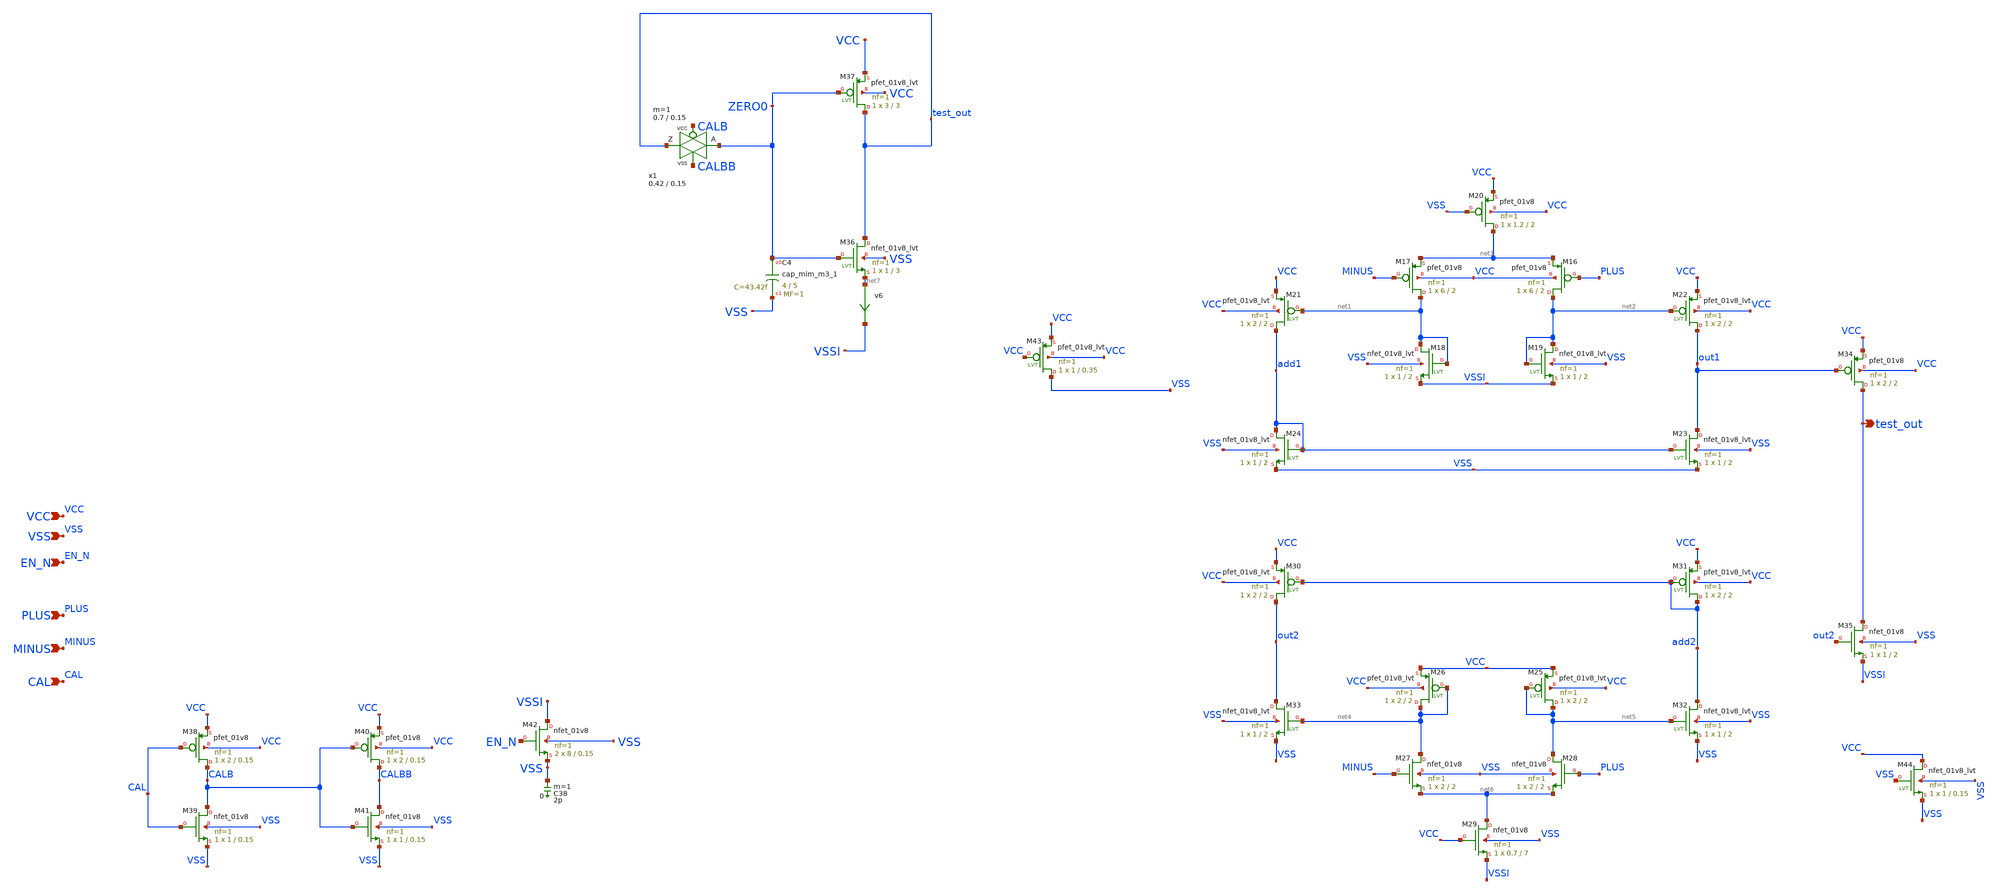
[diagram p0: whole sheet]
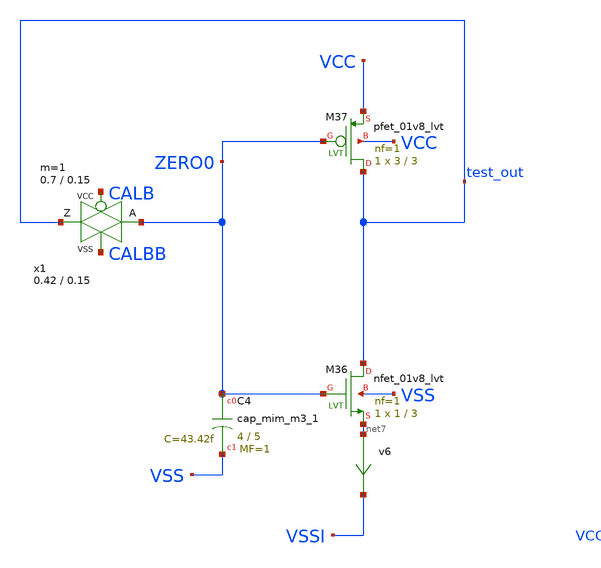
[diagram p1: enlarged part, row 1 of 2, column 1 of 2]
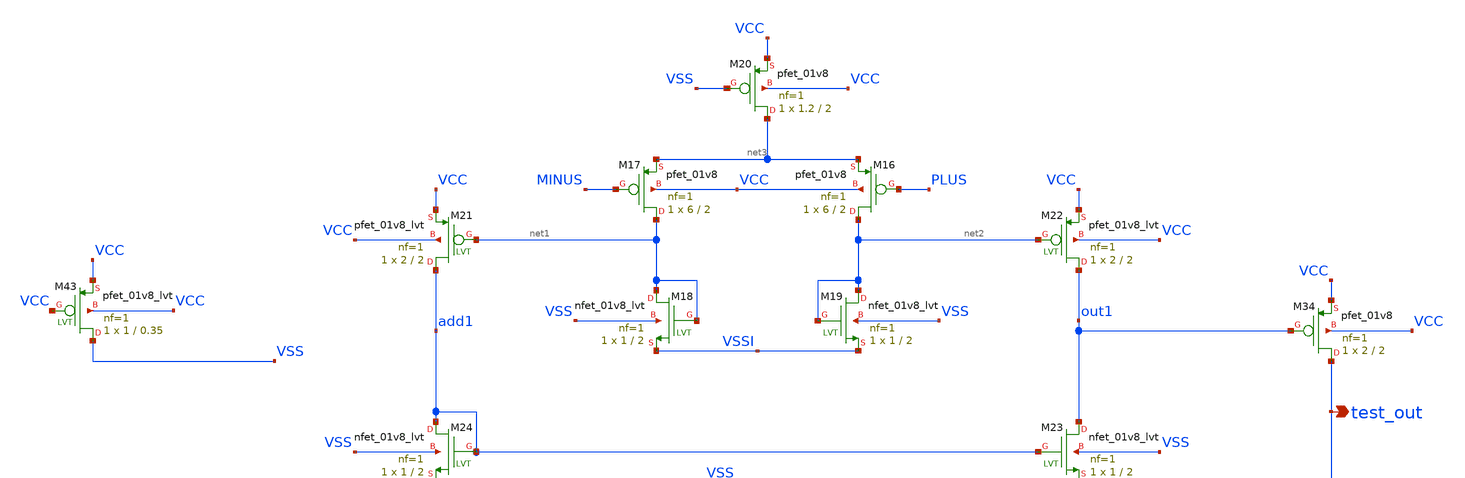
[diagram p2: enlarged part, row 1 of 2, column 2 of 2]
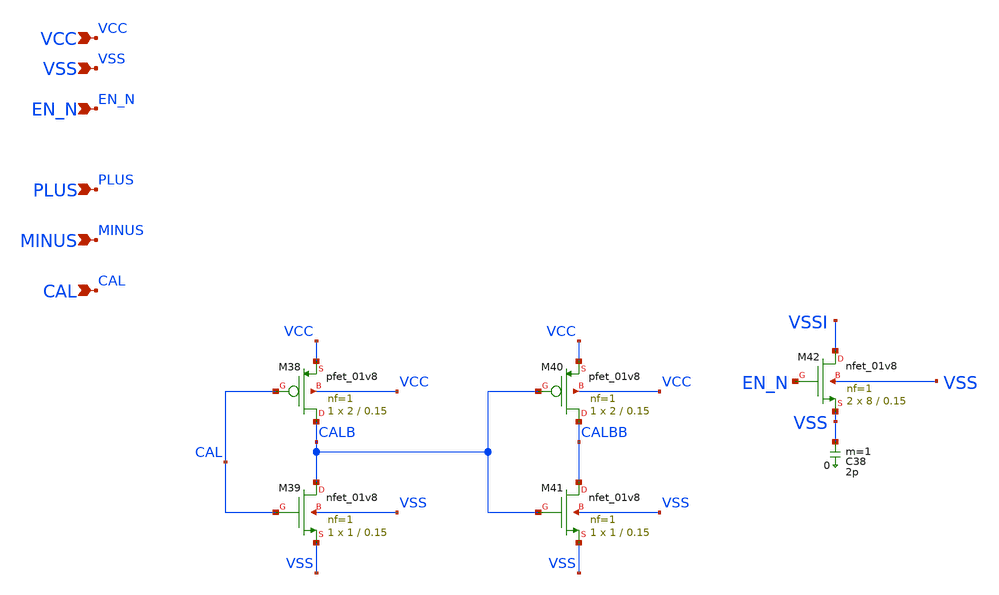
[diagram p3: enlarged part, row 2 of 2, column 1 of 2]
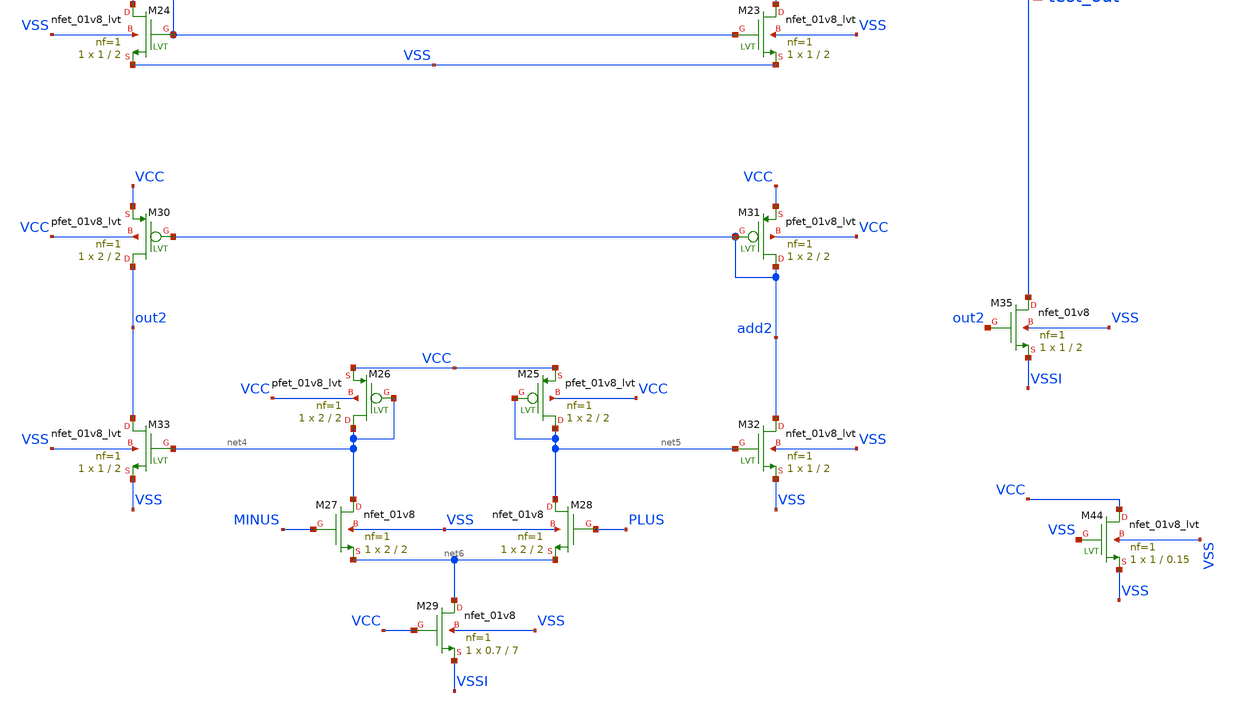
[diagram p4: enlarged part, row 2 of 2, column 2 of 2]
** sch_path: xschem/comparator.sch
**.subckt comparator VCC VSS EN_N PLUS MINUS test_out CAL
*.ipin VCC
*.ipin VSS
*.ipin EN_N
*.ipin PLUS
*.ipin MINUS
*.opin test_out
*.ipin CAL
XM16 net2 PLUS net3 VCC sky130_fd_pr__pfet_01v8 L=2 W=6 nf=1 ad='int((nf+1)/2) * W/nf * 0.29' as='int((nf+2)/2) * W/nf * 0.29'
+ pd='2*int((nf+1)/2) * (W/nf + 0.29)' ps='2*int((nf+2)/2) * (W/nf + 0.29)' nrd='0.29 / W' nrs='0.29 / W'
+ sa=0 sb=0 sd=0 mult=1 m=1
XM17 net1 MINUS net3 VCC sky130_fd_pr__pfet_01v8 L=2 W=6 nf=1 ad='int((nf+1)/2) * W/nf * 0.29' as='int((nf+2)/2) * W/nf * 0.29'
+ pd='2*int((nf+1)/2) * (W/nf + 0.29)' ps='2*int((nf+2)/2) * (W/nf + 0.29)' nrd='0.29 / W' nrs='0.29 / W'
+ sa=0 sb=0 sd=0 mult=1 m=1
XM18 net1 net1 VSSI VSS sky130_fd_pr__nfet_01v8_lvt L=2 W=1 nf=1 ad='int((nf+1)/2) * W/nf * 0.29' as='int((nf+2)/2) * W/nf * 0.29'
+ pd='2*int((nf+1)/2) * (W/nf + 0.29)' ps='2*int((nf+2)/2) * (W/nf + 0.29)' nrd='0.29 / W' nrs='0.29 / W'
+ sa=0 sb=0 sd=0 mult=1 m=1
XM19 net2 net2 VSSI VSS sky130_fd_pr__nfet_01v8_lvt L=2 W=1 nf=1 ad='int((nf+1)/2) * W/nf * 0.29' as='int((nf+2)/2) * W/nf * 0.29'
+ pd='2*int((nf+1)/2) * (W/nf + 0.29)' ps='2*int((nf+2)/2) * (W/nf + 0.29)' nrd='0.29 / W' nrs='0.29 / W'
+ sa=0 sb=0 sd=0 mult=1 m=1
XM20 net3 VSS VCC VCC sky130_fd_pr__pfet_01v8 L=2 W=1.2 nf=1 ad='int((nf+1)/2) * W/nf * 0.29' as='int((nf+2)/2) * W/nf * 0.29'
+ pd='2*int((nf+1)/2) * (W/nf + 0.29)' ps='2*int((nf+2)/2) * (W/nf + 0.29)' nrd='0.29 / W' nrs='0.29 / W'
+ sa=0 sb=0 sd=0 mult=1 m=1
XM21 add1 net1 VCC VCC sky130_fd_pr__pfet_01v8_lvt L=2 W=2 nf=1 ad='int((nf+1)/2) * W/nf * 0.29' as='int((nf+2)/2) * W/nf * 0.29'
+ pd='2*int((nf+1)/2) * (W/nf + 0.29)' ps='2*int((nf+2)/2) * (W/nf + 0.29)' nrd='0.29 / W' nrs='0.29 / W'
+ sa=0 sb=0 sd=0 mult=1 m=1
XM22 out1 net2 VCC VCC sky130_fd_pr__pfet_01v8_lvt L=2 W=2 nf=1 ad='int((nf+1)/2) * W/nf * 0.29' as='int((nf+2)/2) * W/nf * 0.29'
+ pd='2*int((nf+1)/2) * (W/nf + 0.29)' ps='2*int((nf+2)/2) * (W/nf + 0.29)' nrd='0.29 / W' nrs='0.29 / W'
+ sa=0 sb=0 sd=0 mult=1 m=1
XM23 out1 add1 VSS VSS sky130_fd_pr__nfet_01v8_lvt L=2 W=1 nf=1 ad='int((nf+1)/2) * W/nf * 0.29' as='int((nf+2)/2) * W/nf * 0.29'
+ pd='2*int((nf+1)/2) * (W/nf + 0.29)' ps='2*int((nf+2)/2) * (W/nf + 0.29)' nrd='0.29 / W' nrs='0.29 / W'
+ sa=0 sb=0 sd=0 mult=1 m=1
XM24 add1 add1 VSS VSS sky130_fd_pr__nfet_01v8_lvt L=2 W=1 nf=1 ad='int((nf+1)/2) * W/nf * 0.29' as='int((nf+2)/2) * W/nf * 0.29'
+ pd='2*int((nf+1)/2) * (W/nf + 0.29)' ps='2*int((nf+2)/2) * (W/nf + 0.29)' nrd='0.29 / W' nrs='0.29 / W'
+ sa=0 sb=0 sd=0 mult=1 m=1
XM27 net4 MINUS net6 VSS sky130_fd_pr__nfet_01v8 L=2 W=2 nf=1 ad='int((nf+1)/2) * W/nf * 0.29' as='int((nf+2)/2) * W/nf * 0.29'
+ pd='2*int((nf+1)/2) * (W/nf + 0.29)' ps='2*int((nf+2)/2) * (W/nf + 0.29)' nrd='0.29 / W' nrs='0.29 / W'
+ sa=0 sb=0 sd=0 mult=1 m=1
XM28 net5 PLUS net6 VSS sky130_fd_pr__nfet_01v8 L=2 W=2 nf=1 ad='int((nf+1)/2) * W/nf * 0.29' as='int((nf+2)/2) * W/nf * 0.29'
+ pd='2*int((nf+1)/2) * (W/nf + 0.29)' ps='2*int((nf+2)/2) * (W/nf + 0.29)' nrd='0.29 / W' nrs='0.29 / W'
+ sa=0 sb=0 sd=0 mult=1 m=1
XM30 out2 add2 VCC VCC sky130_fd_pr__pfet_01v8_lvt L=2 W=2 nf=1 ad='int((nf+1)/2) * W/nf * 0.29' as='int((nf+2)/2) * W/nf * 0.29'
+ pd='2*int((nf+1)/2) * (W/nf + 0.29)' ps='2*int((nf+2)/2) * (W/nf + 0.29)' nrd='0.29 / W' nrs='0.29 / W'
+ sa=0 sb=0 sd=0 mult=1 m=1
XM31 add2 add2 VCC VCC sky130_fd_pr__pfet_01v8_lvt L=2 W=2 nf=1 ad='int((nf+1)/2) * W/nf * 0.29' as='int((nf+2)/2) * W/nf * 0.29'
+ pd='2*int((nf+1)/2) * (W/nf + 0.29)' ps='2*int((nf+2)/2) * (W/nf + 0.29)' nrd='0.29 / W' nrs='0.29 / W'
+ sa=0 sb=0 sd=0 mult=1 m=1
XM32 add2 net5 VSS VSS sky130_fd_pr__nfet_01v8_lvt L=2 W=1 nf=1 ad='int((nf+1)/2) * W/nf * 0.29' as='int((nf+2)/2) * W/nf * 0.29'
+ pd='2*int((nf+1)/2) * (W/nf + 0.29)' ps='2*int((nf+2)/2) * (W/nf + 0.29)' nrd='0.29 / W' nrs='0.29 / W'
+ sa=0 sb=0 sd=0 mult=1 m=1
XM33 out2 net4 VSS VSS sky130_fd_pr__nfet_01v8_lvt L=2 W=1 nf=1 ad='int((nf+1)/2) * W/nf * 0.29' as='int((nf+2)/2) * W/nf * 0.29'
+ pd='2*int((nf+1)/2) * (W/nf + 0.29)' ps='2*int((nf+2)/2) * (W/nf + 0.29)' nrd='0.29 / W' nrs='0.29 / W'
+ sa=0 sb=0 sd=0 mult=1 m=1
XM29 net6 VCC VSSI VSS sky130_fd_pr__nfet_01v8 L=7 W=0.7 nf=1 ad='int((nf+1)/2) * W/nf * 0.29' as='int((nf+2)/2) * W/nf * 0.29'
+ pd='2*int((nf+1)/2) * (W/nf + 0.29)' ps='2*int((nf+2)/2) * (W/nf + 0.29)' nrd='0.29 / W' nrs='0.29 / W'
+ sa=0 sb=0 sd=0 mult=1 m=1
XM34 test_out out1 VCC VCC sky130_fd_pr__pfet_01v8 L=2 W=2 nf=1 ad='int((nf+1)/2) * W/nf * 0.29' as='int((nf+2)/2) * W/nf * 0.29'
+ pd='2*int((nf+1)/2) * (W/nf + 0.29)' ps='2*int((nf+2)/2) * (W/nf + 0.29)' nrd='0.29 / W' nrs='0.29 / W'
+ sa=0 sb=0 sd=0 mult=1 m=1
XM35 test_out out2 VSSI VSS sky130_fd_pr__nfet_01v8 L=2 W=1 nf=1 ad='int((nf+1)/2) * W/nf * 0.29' as='int((nf+2)/2) * W/nf * 0.29'
+ pd='2*int((nf+1)/2) * (W/nf + 0.29)' ps='2*int((nf+2)/2) * (W/nf + 0.29)' nrd='0.29 / W' nrs='0.29 / W'
+ sa=0 sb=0 sd=0 mult=1 m=1
XM25 net5 net5 VCC VCC sky130_fd_pr__pfet_01v8_lvt L=2 W=2 nf=1 ad='int((nf+1)/2) * W/nf * 0.29' as='int((nf+2)/2) * W/nf * 0.29'
+ pd='2*int((nf+1)/2) * (W/nf + 0.29)' ps='2*int((nf+2)/2) * (W/nf + 0.29)' nrd='0.29 / W' nrs='0.29 / W'
+ sa=0 sb=0 sd=0 mult=1 m=1
XM26 net4 net4 VCC VCC sky130_fd_pr__pfet_01v8_lvt L=2 W=2 nf=1 ad='int((nf+1)/2) * W/nf * 0.29' as='int((nf+2)/2) * W/nf * 0.29'
+ pd='2*int((nf+1)/2) * (W/nf + 0.29)' ps='2*int((nf+2)/2) * (W/nf + 0.29)' nrd='0.29 / W' nrs='0.29 / W'
+ sa=0 sb=0 sd=0 mult=1 m=1
v6 net7 VSSI 0
.save i(v6)
x1 test_out ZERO0 CALB CALBB VCC VSS passgate W_N=0.42 L_N=0.15 W_P=0.7 L_P=0.15 m=1
XC4 ZERO0 VSS sky130_fd_pr__cap_mim_m3_1 W=4 L=5 MF=1 m=1
XM36 test_out ZERO0 net7 VSS sky130_fd_pr__nfet_01v8_lvt L=3 W=1 nf=1 ad='W * 0.29' as='W * 0.29' pd='2*(W + 0.29)'
+ ps='2*(W + 0.29)' nrd=0 nrs=0 sa=0 sb=0 sd=0 mult=1 m=1
XM37 test_out ZERO0 VCC VCC sky130_fd_pr__pfet_01v8_lvt L=3 W=3 nf=1 ad='W * 0.29' as='W * 0.29' pd='2*(W + 0.29)'
+ ps='2*(W + 0.29)' nrd=0 nrs=0 sa=0 sb=0 sd=0 mult=1 m=1
XM38 CALB CAL VCC VCC sky130_fd_pr__pfet_01v8 L=0.15 W=2 nf=1 ad='int((nf+1)/2) * W/nf * 0.29' as='int((nf+2)/2) * W/nf * 0.29'
+ pd='2*int((nf+1)/2) * (W/nf + 0.29)' ps='2*int((nf+2)/2) * (W/nf + 0.29)' nrd='0.29 / W' nrs='0.29 / W'
+ sa=0 sb=0 sd=0 mult=1 m=1
XM39 CALB CAL VSS VSS sky130_fd_pr__nfet_01v8 L=0.15 W=1 nf=1 ad='int((nf+1)/2) * W/nf * 0.29' as='int((nf+2)/2) * W/nf * 0.29'
+ pd='2*int((nf+1)/2) * (W/nf + 0.29)' ps='2*int((nf+2)/2) * (W/nf + 0.29)' nrd='0.29 / W' nrs='0.29 / W'
+ sa=0 sb=0 sd=0 mult=1 m=1
XM40 CALBB CALB VCC VCC sky130_fd_pr__pfet_01v8 L=0.15 W=2 nf=1 ad='int((nf+1)/2) * W/nf * 0.29' as='int((nf+2)/2) * W/nf * 0.29'
+ pd='2*int((nf+1)/2) * (W/nf + 0.29)' ps='2*int((nf+2)/2) * (W/nf + 0.29)' nrd='0.29 / W' nrs='0.29 / W'
+ sa=0 sb=0 sd=0 mult=1 m=1
XM41 CALBB CALB VSS VSS sky130_fd_pr__nfet_01v8 L=0.15 W=1 nf=1 ad='int((nf+1)/2) * W/nf * 0.29' as='int((nf+2)/2) * W/nf * 0.29'
+ pd='2*int((nf+1)/2) * (W/nf + 0.29)' ps='2*int((nf+2)/2) * (W/nf + 0.29)' nrd='0.29 / W' nrs='0.29 / W'
+ sa=0 sb=0 sd=0 mult=1 m=1
C38 VSS 0 2p m=1
XM42 VSSI EN_N VSS VSS sky130_fd_pr__nfet_01v8 L=0.15 W=8 nf=1 ad='W * 0.29' as='W * 0.29' pd='W + 2 * 0.29'
+ ps='W + 2 * 0.29' nrd=0 nrs=0 sa=0 sb=0 sd=0 mult=2 m=2
XM43 VSS VCC VCC VCC sky130_fd_pr__pfet_01v8_lvt L=0.35 W=1 nf=1 ad='int((nf+1)/2) * W/nf * 0.29' as='int((nf+2)/2) * W/nf * 0.29'
+ pd='2*int((nf+1)/2) * (W/nf + 0.29)' ps='2*int((nf+2)/2) * (W/nf + 0.29)' nrd='0.29 / W' nrs='0.29 / W'
+ sa=0 sb=0 sd=0 mult=1 m=1
XM44 VCC VSS VSS VSS sky130_fd_pr__nfet_01v8_lvt L=0.15 W=1 nf=1 ad='int((nf+1)/2) * W/nf * 0.29' as='int((nf+2)/2) * W/nf * 0.29'
+ pd='2*int((nf+1)/2) * (W/nf + 0.29)' ps='2*int((nf+2)/2) * (W/nf + 0.29)' nrd='0.29 / W' nrs='0.29 / W'
+ sa=0 sb=0 sd=0 mult=1 m=1
**.ends

* expanding   symbol:  sky130_tests/passgate.sym # of pins=4
** sym_path: sky130_tests/passgate.sym
** sch_path: sky130_tests/passgate.sch
.subckt passgate Z A GP GN VCCBPIN VSSBPIN  W_N=1 L_N=0.2 W_P=1 L_P=0.2

*.iopin A
*.iopin Z
*.ipin GP
*.ipin GN
XM1 A GN Z VSS sky130_fd_pr__nfet_01v8 W=W_N L=L_N ad='W * 0.29' pd='W + 2 * 0.29' as='W * 0.29' ps='W + 2 * 0.29'
+ nrd=0 nrs=0 sa=0 sb=0 sd=0 nf=1 mult=1
XM2 A GP Z VCC sky130_fd_pr__pfet_01v8 W=W_P L=L_P ad='W * 0.29' pd='W + 2 * 0.29' as='W * 0.29' ps='W + 2 * 0.29'
+ nrd=0 nrs=0 sa=0 sb=0 sd=0 nf=1 mult=1
.ends

.end
